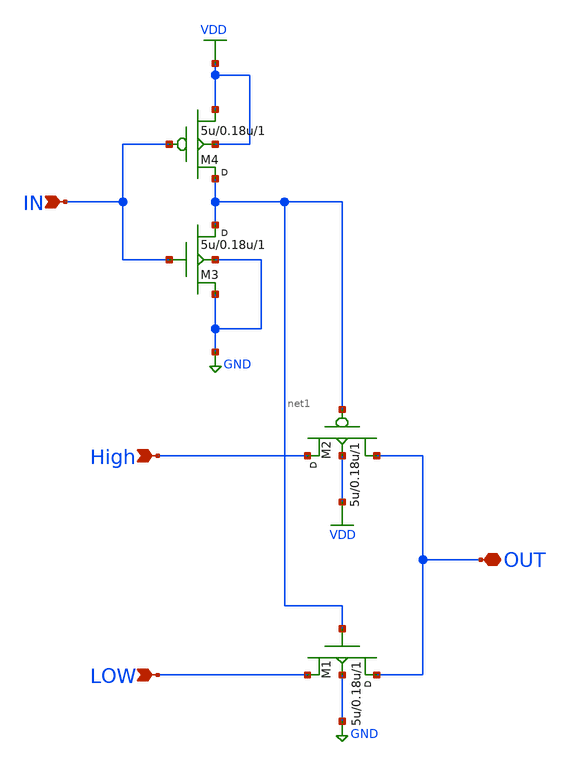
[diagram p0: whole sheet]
** sch_path: LR_Work2/SEL.sch
**.subckt SEL OUT High LOW IN
*.iopin OUT
*.ipin High
*.ipin LOW
*.ipin IN
M1 OUT net1 LOW GND nmos w=5u l=0.18u m=1
M2 High net1 OUT VDD pmos w=5u l=0.18u m=1
M3 net1 IN GND GND nmos w=5u l=0.18u m=1
M4 net1 IN VDD VDD pmos w=5u l=0.18u m=1
**.ends
.GLOBAL GND
.GLOBAL VDD
.end
